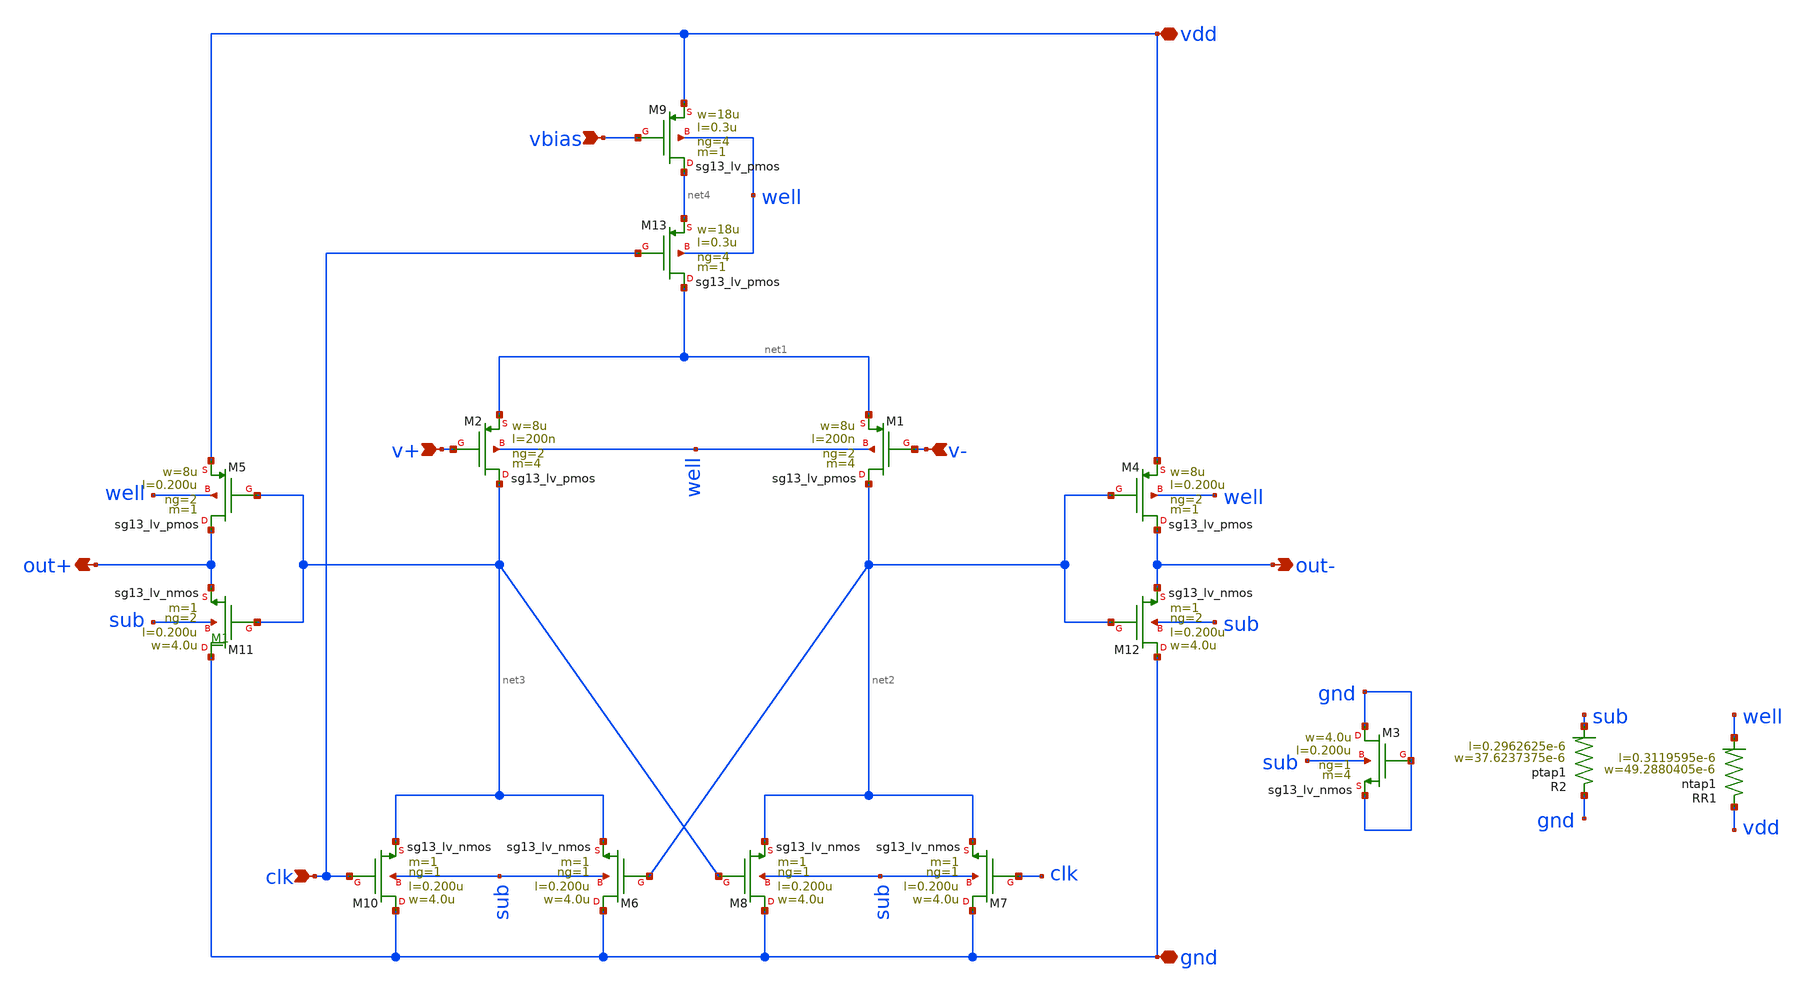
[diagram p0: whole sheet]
** sch_path: part_5_analog_layout/comparator/layout/schematic/DIFF_COMPARATOR.sch
**.subckt DIFF_COMPARATOR vdd gnd v+ v- clk out- out+ vbias
*.iopin vdd
*.iopin gnd
*.ipin v+
*.ipin v-
*.ipin clk
*.opin out-
*.opin out+
*.ipin vbias
XM2 net3 v+ net1 well sg13_lv_pmos w=8u l=200n ng=2 m=4 mm_ok=1
XM1 net2 v- net1 well sg13_lv_pmos w=8u l=200n ng=2 m=4 mm_ok=1
XM4 out- net2 vdd well sg13_lv_pmos w=8u l=0.200u ng=2 m=1 mm_ok=1
XM5 out+ net3 vdd well sg13_lv_pmos w=8u l=0.200u ng=2 m=1 mm_ok=1
XM11 gnd net3 out+ sub sg13_lv_nmos w=4.0u l=0.200u ng=2 m=1 mm_ok=1
XM12 gnd net2 out- sub sg13_lv_nmos w=4.0u l=0.200u ng=2 m=1 mm_ok=1
XM6 gnd net2 net3 sub sg13_lv_nmos w=4.0u l=0.200u ng=1 m=1 mm_ok=1
XM10 gnd clk net3 sub sg13_lv_nmos w=4.0u l=0.200u ng=1 m=1 mm_ok=1
XM7 gnd clk net2 sub sg13_lv_nmos w=4.0u l=0.200u ng=1 m=1 mm_ok=1
XM8 gnd net3 net2 sub sg13_lv_nmos w=4.0u l=0.200u ng=1 m=1 mm_ok=1
XM3 gnd gnd gnd sub sg13_lv_nmos w=4.0u l=0.200u ng=1 m=4 mm_ok=1
XM13 net1 clk net4 well sg13_lv_pmos w=18u l=0.3u ng=4 m=1 mm_ok=1
XM9 net4 vbias vdd well sg13_lv_pmos w=18u l=0.3u ng=4 m=1 mm_ok=1
XR1 vdd well ntap1 R=8.553 w=49.2880405e-6 l=0.3119595e-6
XR2 gnd sub ptap1 R=11.27 w=37.6237375e-6 l=0.2962625e-6
**.ends
.end
